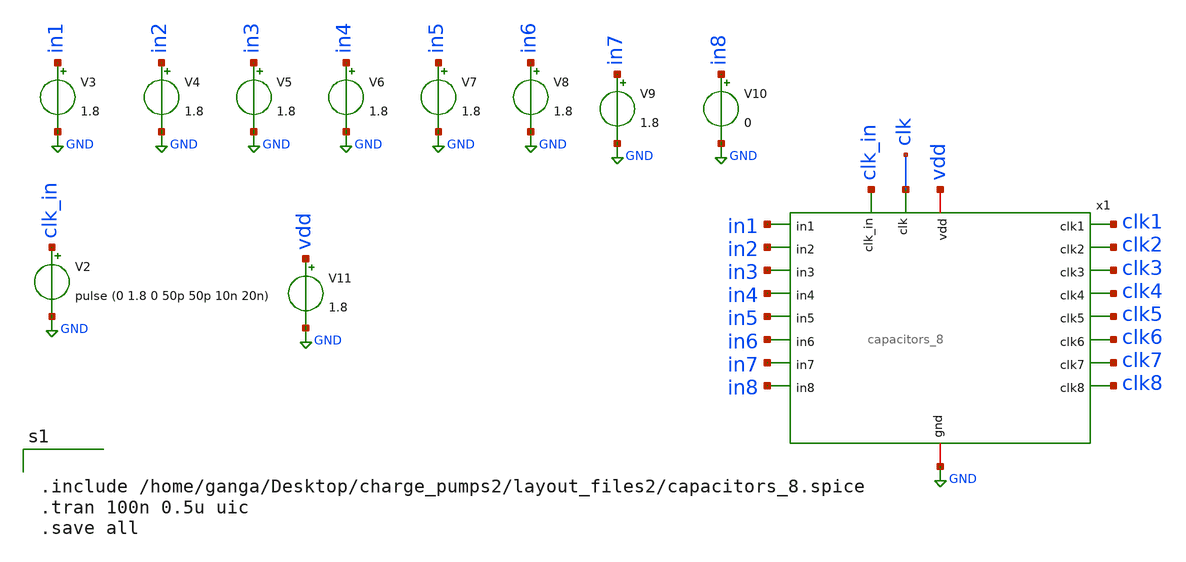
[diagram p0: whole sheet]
** sch_path: xschem/charge_pumps2/capacitors_tb.sch
**.subckt capacitors_tb
x1 GND vdd clk clk8 in8 clk7 clk6 clk4 clk3 clk2 clk1 in1 in2 in3 in4 in5 in6 in7 clk5 clk_in
+ capacitors_8
V3 in1 GND 1.8
V4 in2 GND 1.8
V5 in3 GND 1.8
V6 in4 GND 1.8
V7 in5 GND 1.8
V8 in6 GND 1.8
V9 in7 GND 1.8
V10 in8 GND 0
V2 clk_in GND pulse (0 1.8 0 50p 50p 10n 20n)
V11 vdd GND 1.8
**** begin user architecture code

** opencircuitdesign pdks install
.lib $::SKYWATER_MODELS/sky130.lib.spice tt




.include /home/ganga/Desktop/charge_pumps2/layout_files2/capacitors_8.spice
.tran 100n 0.5u uic
.save all


**** end user architecture code
**.ends
.GLOBAL GND
.end
